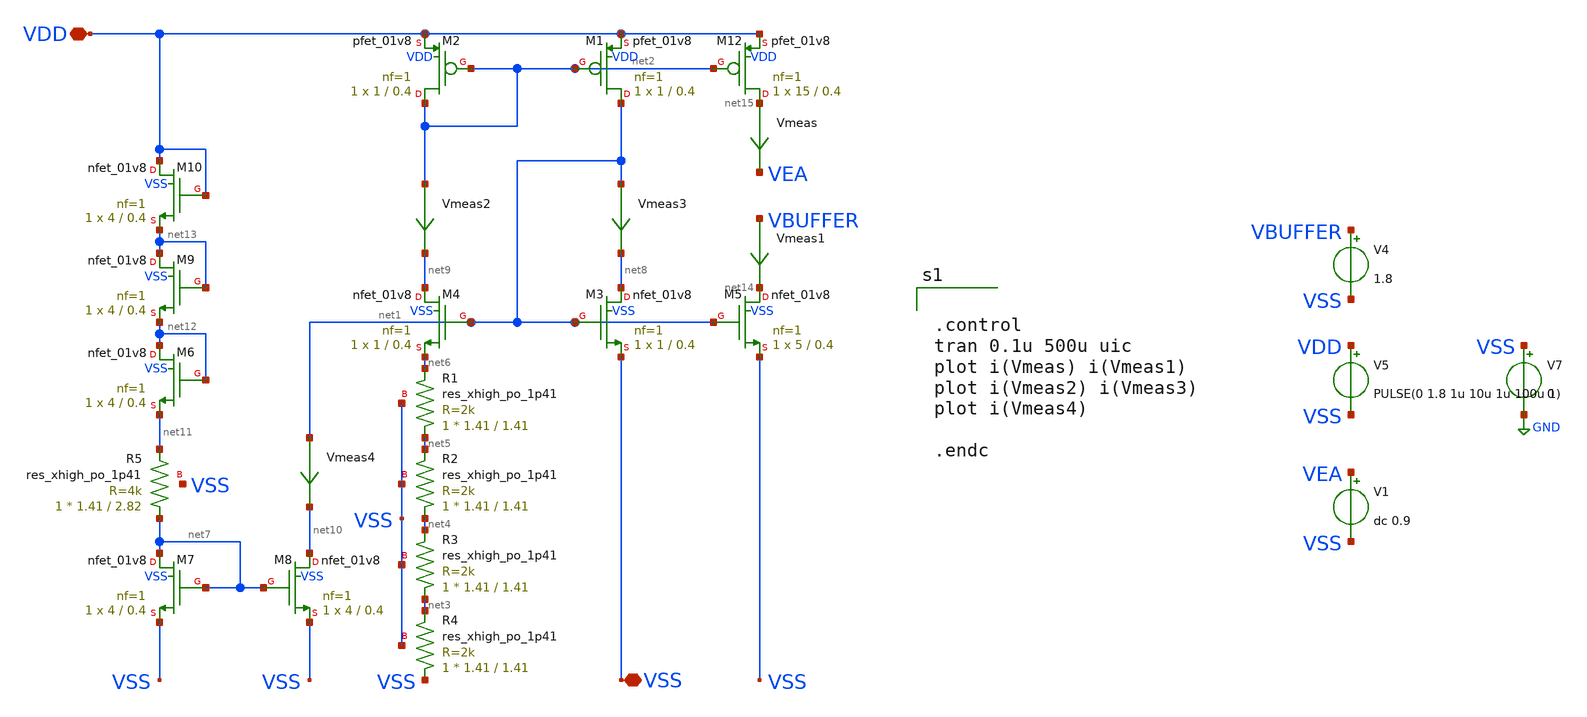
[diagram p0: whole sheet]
** sch_path: xschem/bias-net/testbench/tb_startup.sch
**.subckt tb_startup VSS VDD
*.iopin VSS
*.iopin VDD
XR1 net5 net6 VSS sky130_fd_pr__res_xhigh_po_1p41 L=1.41 mult=1 m=1
XR2 net4 net5 VSS sky130_fd_pr__res_xhigh_po_1p41 L=1.41 mult=1 m=1
XR3 net3 net4 VSS sky130_fd_pr__res_xhigh_po_1p41 L=1.41 mult=1 m=1
XR4 VSS net3 VSS sky130_fd_pr__res_xhigh_po_1p41 L=1.41 mult=1 m=1
XM3 net8 net1 VSS VSS sky130_fd_pr__nfet_01v8 L=0.4 W=1 nf=1 ad='int((nf+1)/2) * W/nf * 0.29' as='int((nf+2)/2) * W/nf * 0.29'
+ pd='2*int((nf+1)/2) * (W/nf + 0.29)' ps='2*int((nf+2)/2) * (W/nf + 0.29)' nrd='0.29 / W' nrs='0.29 / W'
+ sa=0 sb=0 sd=0 mult=1 m=1
XM4 net9 net1 net6 VSS sky130_fd_pr__nfet_01v8 L=0.4 W=1 nf=1 ad='int((nf+1)/2) * W/nf * 0.29' as='int((nf+2)/2) * W/nf * 0.29'
+ pd='2*int((nf+1)/2) * (W/nf + 0.29)' ps='2*int((nf+2)/2) * (W/nf + 0.29)' nrd='0.29 / W' nrs='0.29 / W'
+ sa=0 sb=0 sd=0 mult=1 m=1
XM5 net14 net1 VSS VSS sky130_fd_pr__nfet_01v8 L=0.4 W=5 nf=1 ad='int((nf+1)/2) * W/nf * 0.29' as='int((nf+2)/2) * W/nf * 0.29'
+ pd='2*int((nf+1)/2) * (W/nf + 0.29)' ps='2*int((nf+2)/2) * (W/nf + 0.29)' nrd='0.29 / W' nrs='0.29 / W'
+ sa=0 sb=0 sd=0 mult=1 m=1
Vmeas net15 VEA 0
.save i(vmeas)
Vmeas1 VBUFFER net14 0
.save i(vmeas1)
XM7 net7 net7 VSS VSS sky130_fd_pr__nfet_01v8 L=0.4 W=4 nf=1 ad='int((nf+1)/2) * W/nf * 0.29' as='int((nf+2)/2) * W/nf * 0.29'
+ pd='2*int((nf+1)/2) * (W/nf + 0.29)' ps='2*int((nf+2)/2) * (W/nf + 0.29)' nrd='0.29 / W' nrs='0.29 / W'
+ sa=0 sb=0 sd=0 mult=1 m=1
XM8 net10 net7 VSS VSS sky130_fd_pr__nfet_01v8 L=0.4 W=4 nf=1 ad='int((nf+1)/2) * W/nf * 0.29' as='int((nf+2)/2) * W/nf * 0.29'
+ pd='2*int((nf+1)/2) * (W/nf + 0.29)' ps='2*int((nf+2)/2) * (W/nf + 0.29)' nrd='0.29 / W' nrs='0.29 / W'
+ sa=0 sb=0 sd=0 mult=1 m=1
XR5 net7 net11 VSS sky130_fd_pr__res_xhigh_po_1p41 L=2.82 mult=1 m=1
V5 VDD VSS PULSE(0 1.8 1u 10u 1u 100u 1)
V7 VSS GND 0
V1 VEA VSS dc 0.9
V4 VBUFFER VSS 1.8
Vmeas2 net2 net9 0
.save i(vmeas2)
Vmeas3 net1 net8 0
.save i(vmeas3)
XM1 net1 net2 VDD VDD sky130_fd_pr__pfet_01v8 L=0.4 W=1 nf=1 ad='int((nf+1)/2) * W/nf * 0.29' as='int((nf+2)/2) * W/nf * 0.29'
+ pd='2*int((nf+1)/2) * (W/nf + 0.29)' ps='2*int((nf+2)/2) * (W/nf + 0.29)' nrd='0.29 / W' nrs='0.29 / W'
+ sa=0 sb=0 sd=0 mult=1 m=1
XM2 net2 net2 VDD VDD sky130_fd_pr__pfet_01v8 L=0.4 W=1 nf=1 ad='int((nf+1)/2) * W/nf * 0.29' as='int((nf+2)/2) * W/nf * 0.29'
+ pd='2*int((nf+1)/2) * (W/nf + 0.29)' ps='2*int((nf+2)/2) * (W/nf + 0.29)' nrd='0.29 / W' nrs='0.29 / W'
+ sa=0 sb=0 sd=0 mult=1 m=1
XM12 net15 net2 VDD VDD sky130_fd_pr__pfet_01v8 L=0.4 W=15 nf=1 ad='int((nf+1)/2) * W/nf * 0.29' as='int((nf+2)/2) * W/nf * 0.29'
+ pd='2*int((nf+1)/2) * (W/nf + 0.29)' ps='2*int((nf+2)/2) * (W/nf + 0.29)' nrd='0.29 / W' nrs='0.29 / W'
+ sa=0 sb=0 sd=0 mult=1 m=1
Vmeas4 net1 net10 0
.save i(vmeas4)
XM6 net12 net12 net11 VSS sky130_fd_pr__nfet_01v8 L=0.4 W=4 nf=1 ad='int((nf+1)/2) * W/nf * 0.29' as='int((nf+2)/2) * W/nf * 0.29'
+ pd='2*int((nf+1)/2) * (W/nf + 0.29)' ps='2*int((nf+2)/2) * (W/nf + 0.29)' nrd='0.29 / W' nrs='0.29 / W'
+ sa=0 sb=0 sd=0 mult=1 m=1
XM9 net13 net13 net12 VSS sky130_fd_pr__nfet_01v8 L=0.4 W=4 nf=1 ad='int((nf+1)/2) * W/nf * 0.29' as='int((nf+2)/2) * W/nf * 0.29'
+ pd='2*int((nf+1)/2) * (W/nf + 0.29)' ps='2*int((nf+2)/2) * (W/nf + 0.29)' nrd='0.29 / W' nrs='0.29 / W'
+ sa=0 sb=0 sd=0 mult=1 m=1
XM10 VDD VDD net13 VSS sky130_fd_pr__nfet_01v8 L=0.4 W=4 nf=1 ad='int((nf+1)/2) * W/nf * 0.29' as='int((nf+2)/2) * W/nf * 0.29'
+ pd='2*int((nf+1)/2) * (W/nf + 0.29)' ps='2*int((nf+2)/2) * (W/nf + 0.29)' nrd='0.29 / W' nrs='0.29 / W'
+ sa=0 sb=0 sd=0 mult=1 m=1
**** begin user architecture code


.control
tran 0.1u 500u uic
plot i(Vmeas) i(Vmeas1)
plot i(Vmeas2) i(Vmeas3)
plot i(Vmeas4)

.endc



** opencircuitdesign pdks install
.lib $::SKYWATER_MODELS/sky130.lib.spice tt


**** end user architecture code
**.ends
.GLOBAL GND
.end
